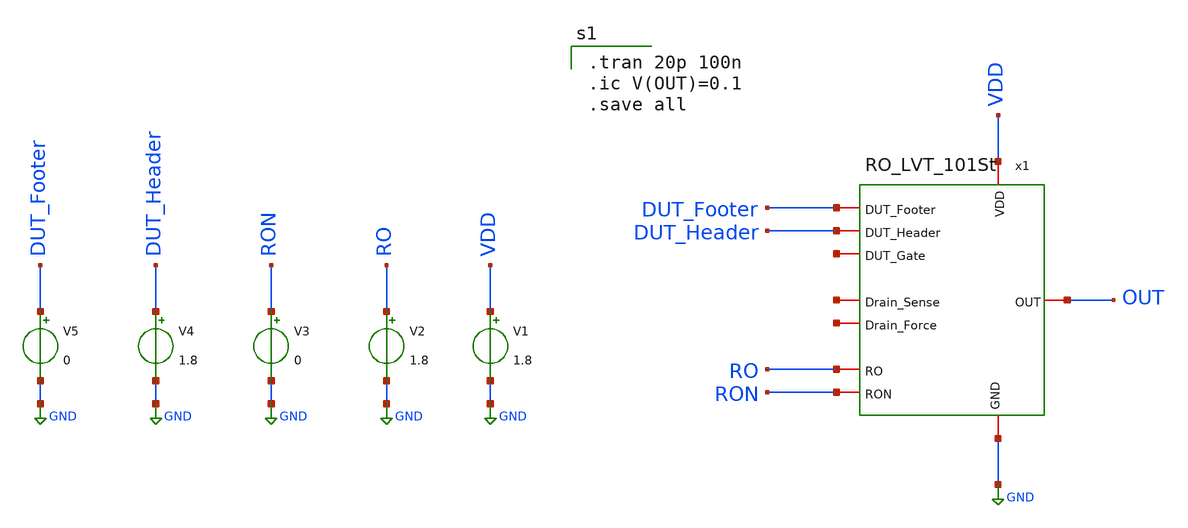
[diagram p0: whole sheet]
** sch_path: TB/RingTB.sch
**.subckt RingTB
V1 VDD GND 1.8
V2 RO GND 1.8
V3 RON GND 0
V4 DUT_Header GND 1.8
V5 DUT_Footer GND 0
x1 VDD GND DUT_Footer DUT_Header net1 net2 RO RON net3 OUT RO_LVT_101St
**** begin user architecture code

** opencircuitdesign pdks install
.lib $::SKYWATER_MODELS/sky130.lib.spice tt



.tran 20p 100n
.ic V(OUT)=0.1
.save all

**** end user architecture code
**.ends
.GLOBAL GND
.GLOBAL VDD
.GLOBAL RO
.GLOBAL RON
.GLOBAL DUT_Header
.GLOBAL DUT_Footer
.end
